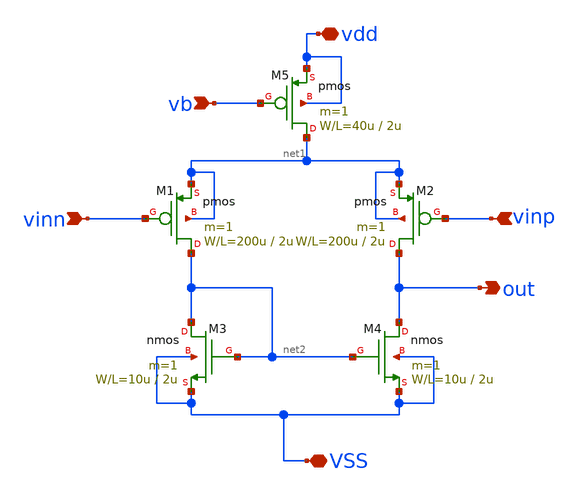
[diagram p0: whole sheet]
** sch_path: member_project/GroupWork/Team_Ando/ugeugeHigh/diffwl500-4.sch
**.subckt diffwl500-4 vinn vinp VSS vdd vb out
*.ipin vinn
*.ipin vinp
*.iopin VSS
*.iopin vdd
*.ipin vb
*.opin out
M5 net1 vb vdd vdd pmos L=2u W=40u m=1
M3 net2 net2 VSS VSS nmos L=2u W=10u m=1
M1 net2 vinn net1 net1 pmos L=2u W=200u m=1
M2 out vinp net1 net1 pmos L=2u W=200u m=1
M4 out net2 VSS VSS nmos L=2u W=10u m=1
**** begin user architecture code
 .include $::LIB/mos.lib
.include $::LIB/passive.lib
.include $::LIB/diode.lib
**** end user architecture code
**.ends
.end
